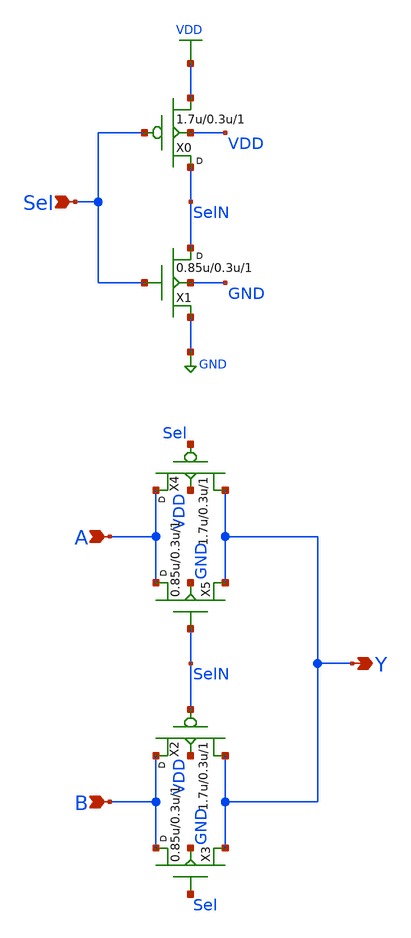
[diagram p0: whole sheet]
** sch_path: openfasoc/common/platforms/gf180mcuosu9Tmux21/gf180mcu_osu_sc_mux2_1.sch
**.subckt gf180mcu_osu_sc_mux2_1 Sel A B Y
*.ipin Sel
*.ipin A
*.ipin B
*.opin Y
X0 SelN Sel VDD VDD pmos_3p3 w=1.7u l=0.3u m=1
X1 SelN Sel GND GND nmos_3p3 w=0.85u l=0.3u m=1
X2 B SelN Y VDD pmos_3p3 w=1.7u l=0.3u m=1
X3 B Sel Y GND nmos_3p3 w=0.85u l=0.3u m=1
X4 A Sel Y VDD pmos_3p3 w=1.7u l=0.3u m=1
X5 A SelN Y GND nmos_3p3 w=0.85u l=0.3u m=1
**.ends
.GLOBAL VDD
.GLOBAL GND
.end
